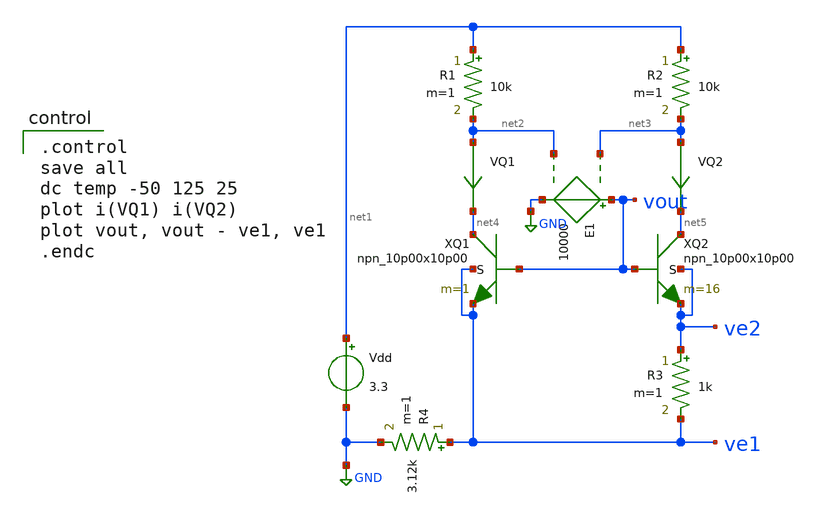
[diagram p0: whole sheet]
** sch_path: bgr/bgr-bjt-tcomp.sch
**.subckt bgr-bjt-tcomp
XQ1 net4 vout ve1 ve1 npn_10p00x10p00 m=1
Vdd net1 GND 3.3
XQ2 net5 vout ve2 ve2 npn_10p00x10p00 m=16
R3 ve2 ve1 1k m=1
R1 net1 net2 10k m=1
R2 net1 net3 10k m=1
E1 vout GND net3 net2 10000
VQ1 net2 net4 0
.save i(vq1)
VQ2 net3 net5 0
.save i(vq2)
R4 ve1 GND 3.12k m=1
**** begin user architecture code

.include $::180MCU_MODELS/design.ngspice
.lib $::180MCU_MODELS/sm141064.ngspice typical
.lib $::180MCU_MODELS/sm141064.ngspice res_typical
.lib $::180MCU_MODELS/sm141064.ngspice moscap_typical
.lib $::180MCU_MODELS/sm141064.ngspice bjt_typical
* .lib $::180MCU_MODELS/sm141064.ngspice res_statistical


.control
save all
dc temp -50 125 25
plot i(VQ1) i(VQ2)
plot vout, vout - ve1, ve1
.endc

**** end user architecture code
**.ends
.GLOBAL GND
.end
